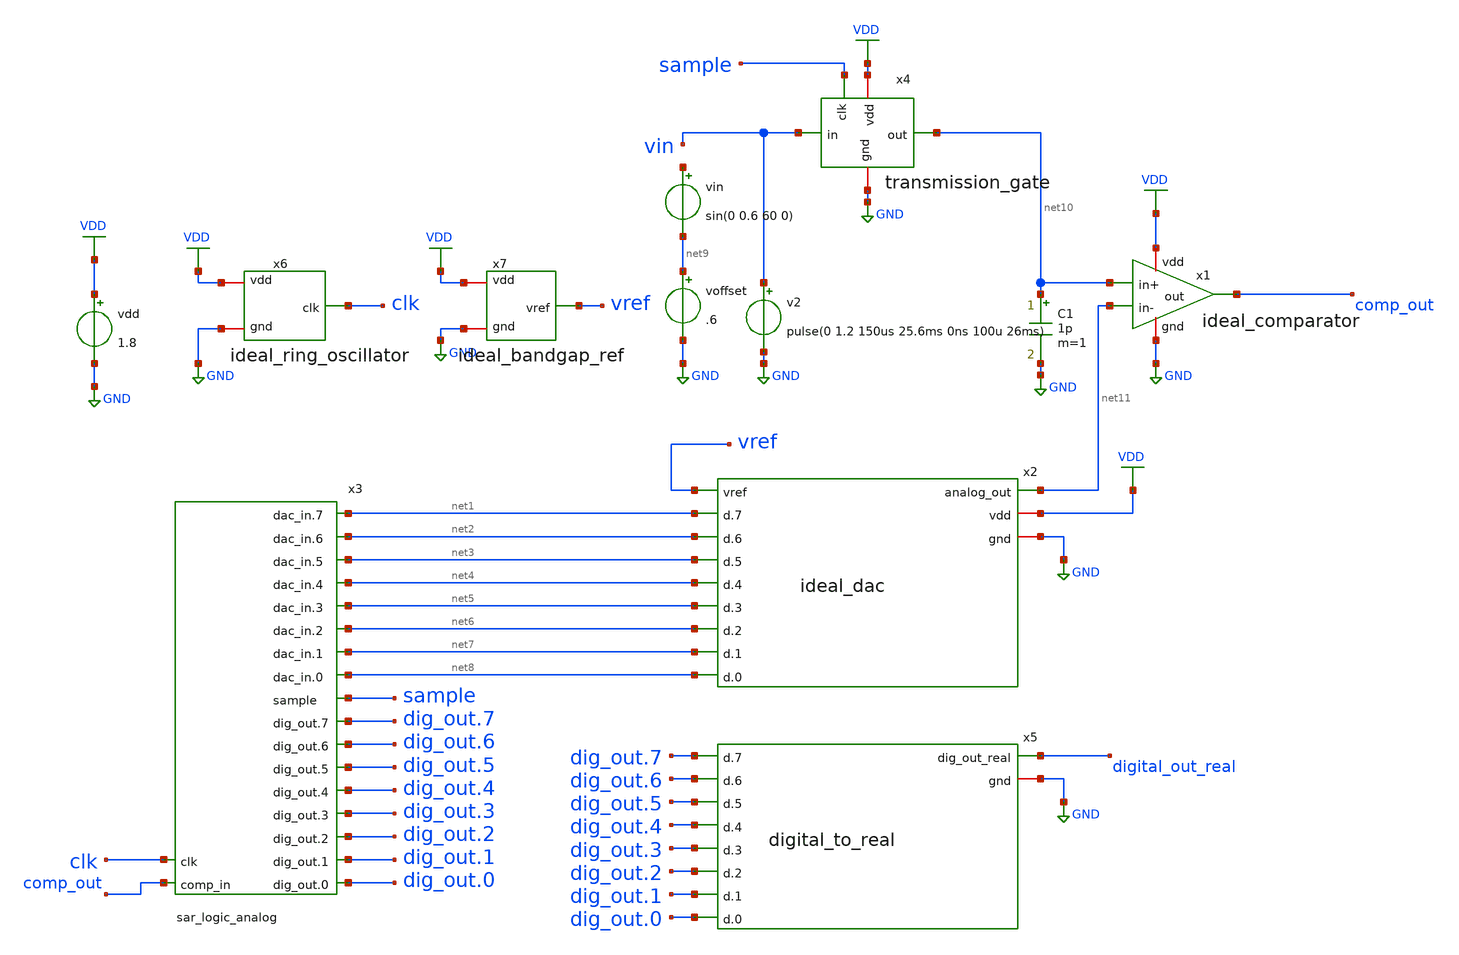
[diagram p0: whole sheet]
** sch_path: ideal_sar_adc.sch
**.subckt ideal_sar_adc
x3 comp_out clk dig_out.0 dig_out.1 dig_out.2 dig_out.3 dig_out.4 dig_out.5 dig_out.6 dig_out.7
+ sample net8 net7 net6 net5 net4 net3 net2 net1 sar_logic_analog
vdd VDD GND 1.8
x1 VDD comp_out net10 net11 GND ideal_comparator
voffset net9 GND .6
vin net12 net9 sin(0 0.6 60 0)
C1 net10 GND 1p m=1
x2 net11 VDD vref GND net3 net2 net6 net4 net1 net5 net7 net8 ideal_dac
x5 digital_out_real dig_out.7 dig_out.6 dig_out.5 dig_out.4 dig_out.3 dig_out.2 dig_out.1 dig_out.0
+ GND digital_to_real
x6 clk VDD GND ideal_ring_oscillator
x7 vref VDD GND ideal_bandgap_ref
x4 VDD sample vin net10 GND transmission_gate
v2 vin GND pulse(0 1.2 150us 25.6ms 0ns 100u 26ms)
**** begin user architecture code


.lib /foss/pdks/sky130A/libs.tech/ngspice/sky130.lib.spice tt


.control
tran 100ns 30ms //16ms
plot v(digital_out_real) v(vin)
save all
run
write /foss/designs/sar_adc/ideal_sar_adc.raw
.endc



**** end user architecture code
**.ends
.GLOBAL GND
.GLOBAL VDD
.end
